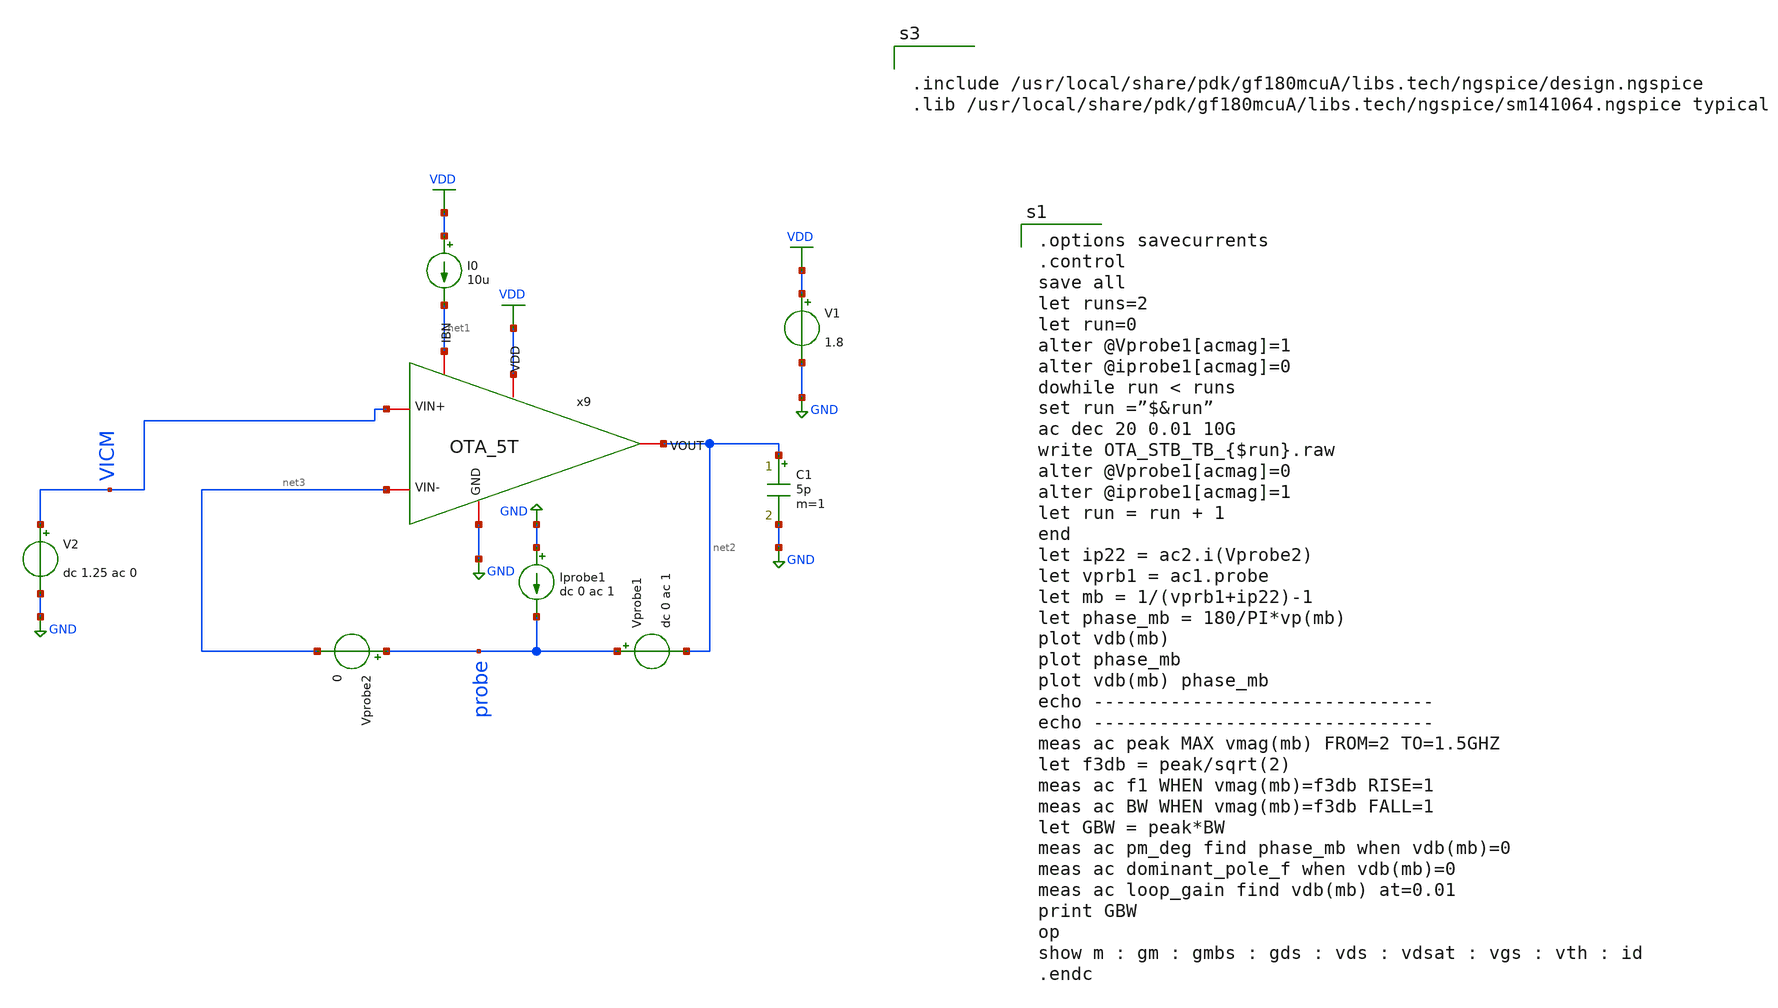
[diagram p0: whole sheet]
** sch_path: lab7_closed_loop.sch
**.subckt lab7_closed_loop
V1 VDD GND 1.8
.save i(v1)
C1 net2 GND 5p m=1
I0 VDD net1 10u
V2 VICM GND dc 1.25 ac 0
.save i(v2)
x9 VDD net2 net3 VICM net1 GND OTA_5T
Vprobe2 probe net3 0
.save i(vprobe2)
Vprobe1 probe net2 dc 0 ac 1
.save i(vprobe1)
Iprobe1 GND probe dc 0 ac 1
**** begin user architecture code


.include /usr/local/share/pdk/gf180mcuA/libs.tech/ngspice/design.ngspice
.lib /usr/local/share/pdk/gf180mcuA/libs.tech/ngspice/sm141064.ngspice typical



.options savecurrents
.control
save all
let runs=2
let run=0
alter @Vprobe1[acmag]=1
alter @iprobe1[acmag]=0
dowhile run < runs
set run =”$&run”
ac dec 20 0.01 10G
write OTA_STB_TB_{$run}.raw
alter @Vprobe1[acmag]=0
alter @iprobe1[acmag]=1
let run = run + 1
end
let ip22 = ac2.i(Vprobe2)
let vprb1 = ac1.probe
let mb = 1/(vprb1+ip22)-1
let phase_mb = 180/PI*vp(mb)
plot vdb(mb)
plot phase_mb
plot vdb(mb) phase_mb
echo -------------------------------
echo -------------------------------
meas ac peak MAX vmag(mb) FROM=2 TO=1.5GHZ
let f3db = peak/sqrt(2)
meas ac f1 WHEN vmag(mb)=f3db RISE=1
meas ac BW WHEN vmag(mb)=f3db FALL=1
let GBW = peak*BW
meas ac pm_deg find phase_mb when vdb(mb)=0
meas ac dominant_pole_f when vdb(mb)=0
meas ac loop_gain find vdb(mb) at=0.01
print GBW
op
show m : gm : gmbs : gds : vds : vdsat : vgs : vth : id
.endc


**** end user architecture code
**.ends

* expanding   symbol:  OTA_5T.sym # of pins=6
** sym_path: OTA_5T.sym
** sch_path: OTA_5T.sch
.subckt OTA_5T VDD VOUT VIN- VIN+ IBN GND
*.iopin VDD
*.iopin GND
*.iopin VIN-
*.iopin VIN+
*.iopin VOUT
*.iopin IBN
XM1 net2 VIN+ net1 GND nfet_03v3 L=450n W=22.27u nf=1 ad='int((nf+1)/2) * W/nf * 0.18u' as='int((nf+2)/2) * W/nf * 0.18u'
+ pd='2*int((nf+1)/2) * (W/nf + 0.18u)' ps='2*int((nf+2)/2) * (W/nf + 0.18u)' nrd='0.18u / W' nrs='0.18u / W'
+ sa=0 sb=0 sd=0 m=1
XM2 VOUT VIN- net1 GND nfet_03v3 L=450n W=22.27u nf=1 ad='int((nf+1)/2) * W/nf * 0.18u' as='int((nf+2)/2) * W/nf * 0.18u'
+ pd='2*int((nf+1)/2) * (W/nf + 0.18u)' ps='2*int((nf+2)/2) * (W/nf + 0.18u)' nrd='0.18u / W' nrs='0.18u / W'
+ sa=0 sb=0 sd=0 m=1
XM4 IBN IBN GND GND nfet_03v3 L=2.7u W=18.15u nf=1 ad='int((nf+1)/2) * W/nf * 0.18u' as='int((nf+2)/2) * W/nf * 0.18u'
+ pd='2*int((nf+1)/2) * (W/nf + 0.18u)' ps='2*int((nf+2)/2) * (W/nf + 0.18u)' nrd='0.18u / W' nrs='0.18u / W'
+ sa=0 sb=0 sd=0 m=1
XM5 VOUT net2 VDD VDD pfet_03v3 L=300n W=5.84u nf=1 ad='int((nf+1)/2) * W/nf * 0.18u' as='int((nf+2)/2) * W/nf * 0.18u'
+ pd='2*int((nf+1)/2) * (W/nf + 0.18u)' ps='2*int((nf+2)/2) * (W/nf + 0.18u)' nrd='0.18u / W' nrs='0.18u / W'
+ sa=0 sb=0 sd=0 m=1
XM6 net2 net2 VDD VDD pfet_03v3 L=300n W=5.84u nf=1 ad='int((nf+1)/2) * W/nf * 0.18u' as='int((nf+2)/2) * W/nf * 0.18u'
+ pd='2*int((nf+1)/2) * (W/nf + 0.18u)' ps='2*int((nf+2)/2) * (W/nf + 0.18u)' nrd='0.18u / W' nrs='0.18u / W'
+ sa=0 sb=0 sd=0 m=1
XM3 net1 IBN GND GND nfet_03v3 L=2.7u W=72.6u nf=1 ad='int((nf+1)/2) * W/nf * 0.18u' as='int((nf+2)/2) * W/nf * 0.18u'
+ pd='2*int((nf+1)/2) * (W/nf + 0.18u)' ps='2*int((nf+2)/2) * (W/nf + 0.18u)' nrd='0.18u / W' nrs='0.18u / W'
+ sa=0 sb=0 sd=0 m=1
.ends

.GLOBAL GND
.GLOBAL VDD
.end
